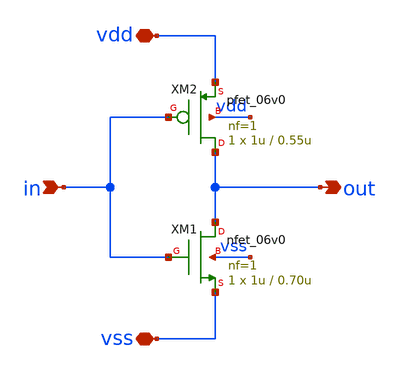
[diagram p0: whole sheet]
** sch_path: xschem/logic/inv_lvt.sch
**.subckt inv_lvt vdd vss in out
*.iopin vdd
*.iopin vss
*.ipin in
*.opin out
XM1 out in vss vss nfet_06v0 L=0.70u W=1u nf=1 ad='int((nf+1)/2) * W/nf * 0.18u' as='int((nf+2)/2) * W/nf * 0.18u'
+ pd='2*int((nf+1)/2) * (W/nf + 0.18u)' ps='2*int((nf+2)/2) * (W/nf + 0.18u)' nrd='0.18u / W' nrs='0.18u / W'
+ sa=0 sb=0 sd=0 m=1
XM2 out in vdd vdd pfet_06v0 L=0.55u W=1u nf=1 ad='int((nf+1)/2) * W/nf * 0.18u' as='int((nf+2)/2) * W/nf * 0.18u'
+ pd='2*int((nf+1)/2) * (W/nf + 0.18u)' ps='2*int((nf+2)/2) * (W/nf + 0.18u)' nrd='0.18u / W' nrs='0.18u / W'
+ sa=0 sb=0 sd=0 m=1
**.ends
.end
